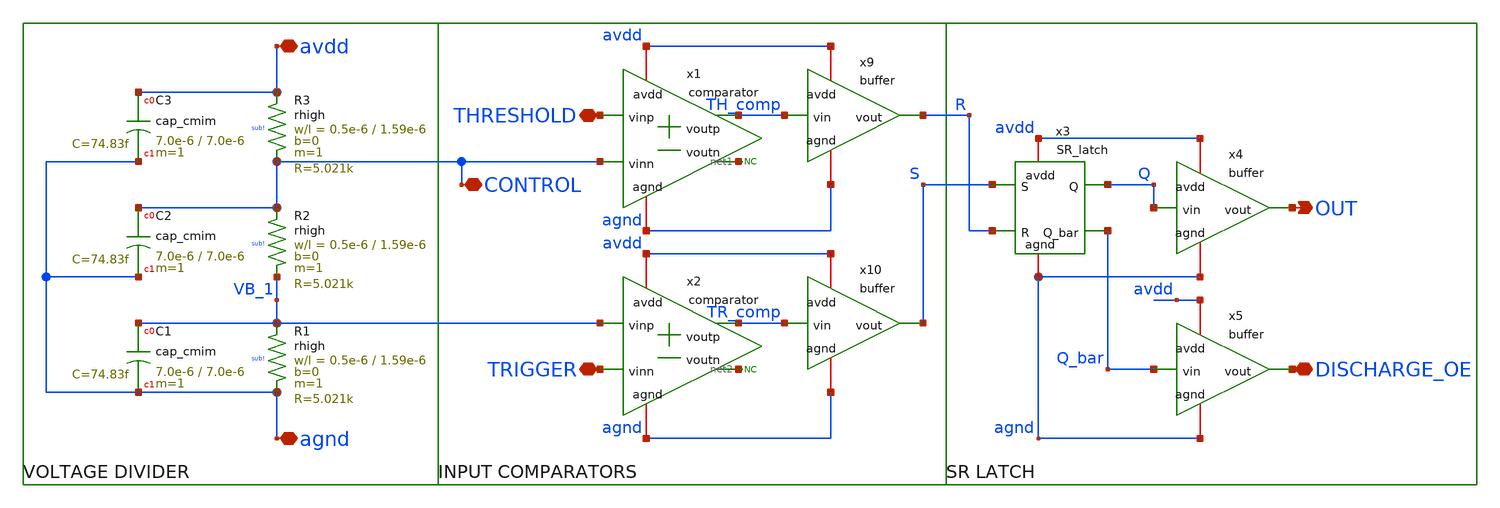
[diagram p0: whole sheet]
** sch_path: xschem/555.sch
**.subckt 555 OUT avdd agnd TRIGGER THRESHOLD DISCHARGE_OE CONTROL
*.opin OUT
*.iopin avdd
*.iopin agnd
*.iopin TRIGGER
*.iopin THRESHOLD
*.iopin DISCHARGE_OE
*.iopin CONTROL
XR3 avdd CONTROL sub! rhigh w=0.5e-6 l=1.59e-6 m=1 b=0 mm_ok=1
XR1 VB_1 agnd sub! rhigh w=0.5e-6 l=1.59e-6 m=1 b=0 mm_ok=1
XR2 CONTROL VB_1 sub! rhigh w=0.5e-6 l=1.59e-6 m=1 b=0 mm_ok=1
XC1 VB_1 agnd cap_cmim w=7.0e-6 l=7.0e-6 m=1 mm_ok=1
XC2 CONTROL agnd cap_cmim w=7.0e-6 l=7.0e-6 m=1 mm_ok=1
XC3 avdd agnd cap_cmim w=7.0e-6 l=7.0e-6 m=1 mm_ok=1
x1 avdd TH_comp net1 CONTROL THRESHOLD agnd comparator
x2 avdd TR_comp net2 TRIGGER VB_1 agnd comparator
x9 avdd TH_comp R agnd buffer
x10 avdd TR_comp S agnd buffer
x3 avdd Q_bar Q agnd S R SR_latch
x4 avdd Q OUT agnd buffer
x5 avdd Q_bar DISCHARGE_OE agnd buffer
* noconn #net1
* noconn #net2
**.ends

* expanding   symbol:  comparator.sym # of pins=6
** sym_path: xschem/comparator.sym
** sch_path: xschem/comparator.sch
.subckt comparator avdd voutp voutn vinn vinp agnd
*.iopin avdd
*.ipin vinp
*.opin voutp
*.iopin agnd
*.ipin vinn
*.opin voutn
XQ1 voutp vinn ee agnd npn13G2 Nx=1 mm_ok=1
XR1 avdd voutp sub! rppd w=0.5e-6 l=20e-6 m=1 b=0 mm_ok=1
XR2 ee agnd sub! rppd w=0.5e-6 l=2e-6 m=1 b=0 mm_ok=1
XR3 avdd voutn sub! rppd w=0.5e-6 l=20e-6 m=1 b=0 mm_ok=1
XQ2 voutn vinp ee agnd npn13G2 Nx=1 mm_ok=1
.ends


* expanding   symbol:  buffer.sym # of pins=4
** sym_path: xschem/buffer.sym
** sch_path: xschem/buffer.sch
.subckt buffer avdd vin vout agnd
*.iopin avdd
*.ipin vin
*.opin vout
*.iopin agnd
x1 avdd vin net1 agnd inverter
x2 avdd net1 vout agnd inverter
.ends


* expanding   symbol:  SR_latch.sym # of pins=6
** sym_path: xschem/SR_latch.sym
** sch_path: xschem/SR_latch.sch
.subckt SR_latch avdd Q_bar Q agnd S R
*.ipin R
*.opin Q_bar
*.ipin S
*.opin Q
*.iopin avdd
*.iopin agnd
XQ2 Q_bar net2 agnd agnd npn13G2 Nx=1 mm_ok=1
XQ1 Q net1 agnd agnd npn13G2 Nx=1 mm_ok=1
XR3 net1 R sub! rppd w=0.5e-6 l=20e-6 m=1 b=0 mm_ok=1
XR1 S net2 sub! rppd w=0.5e-6 l=20e-6 m=1 b=0 mm_ok=1
XR2 net1 agnd sub! rhigh w=0.5e-6 l=20e-6 m=1 b=0 mm_ok=1
XR4 net2 agnd sub! rhigh w=0.5e-6 l=20e-6 m=1 b=0 mm_ok=1
XR5 net2 Q sub! rppd w=0.5e-6 l=20e-6 m=1 b=0 mm_ok=1
XR6 Q_bar net1 sub! rppd w=0.5e-6 l=20e-6 m=1 b=0 mm_ok=1
XR7 avdd Q sub! rppd w=0.5e-6 l=2e-6 m=1 b=0 mm_ok=1
XR8 avdd Q_bar sub! rppd w=0.5e-6 l=2e-6 m=1 b=0 mm_ok=1
.ends


* expanding   symbol:  inverter.sym # of pins=4
** sym_path: xschem/inverter.sym
** sch_path: xschem/inverter.sch
.subckt inverter avdd vin vout agnd
*.iopin avdd
*.ipin vin
*.opin vout
*.iopin agnd
XQ1 vout base agnd agnd npn13G2 Nx=10 mm_ok=1
XR1 avdd vout sub! rhigh w=1e-6 l=0.5e-6 m=1 b=0 mm_ok=1
XR2 base vin sub! rhigh w=0.5e-6 l=0.5e-6 m=1 b=0 mm_ok=1
.ends

.end
